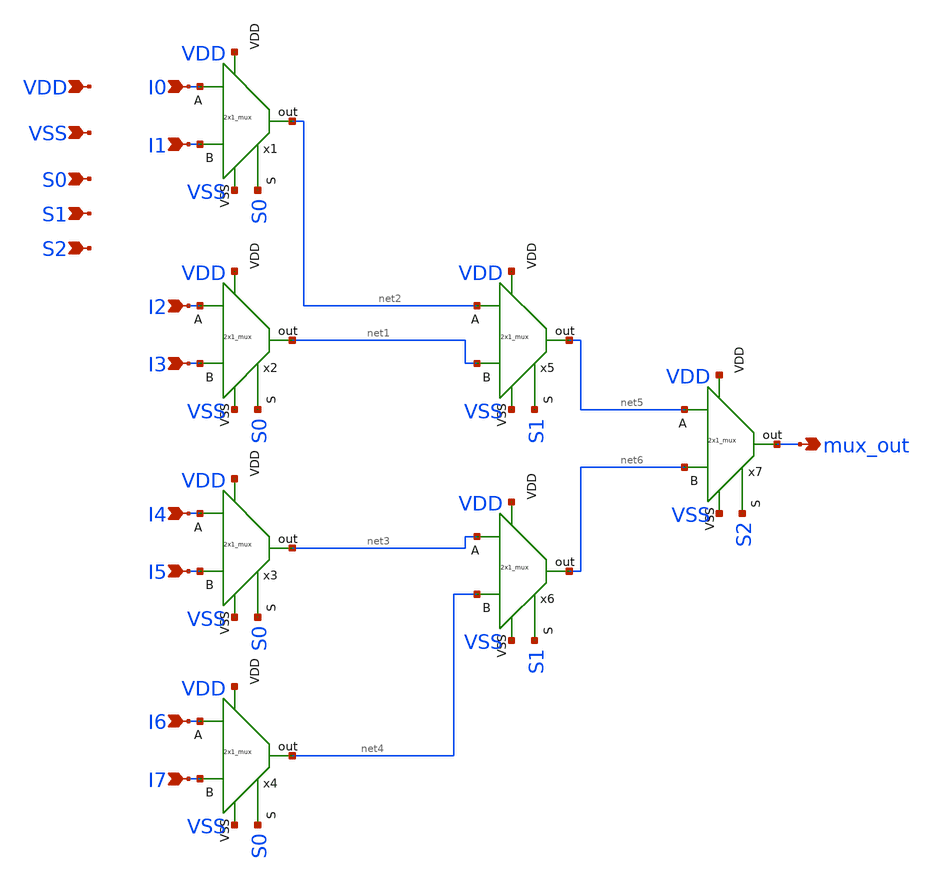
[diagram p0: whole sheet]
** sch_path: 8bit_mux.sch
**.subckt 8bit_mux I0 I1 I2 I3 I4 I5 I6 I7 VDD VSS S0 S1 S2 mux_out
*.ipin I0
*.ipin I1
*.ipin I2
*.ipin I3
*.ipin I4
*.ipin I5
*.ipin I6
*.ipin I7
*.ipin VDD
*.ipin VSS
*.ipin S0
*.ipin S1
*.ipin S2
*.opin mux_out
x1 I1 VDD I0 VSS S0 net2 2x1_mux
x2 I3 VDD I2 VSS S0 net1 2x1_mux
x3 I5 VDD I4 VSS S0 net3 2x1_mux
x4 I7 VDD I6 VSS S0 net4 2x1_mux
x5 net1 VDD net2 VSS S1 net5 2x1_mux
x6 net4 VDD net3 VSS S1 net6 2x1_mux
x7 net6 VDD net5 VSS S2 mux_out 2x1_mux
**.ends

* expanding   symbol:  2x1_mux/2x1_mux.sym # of pins=6
** sym_path: 2x1_mux/2x1_mux.sym
** sch_path: 2x1_mux/2x1_mux.sch
.subckt 2x1_mux B VDD A VSS S out
*.ipin VDD
*.ipin A
*.ipin B
*.opin out
*.ipin S
*.ipin VSS
XM1 net1 A net4 net4 sky130_fd_pr__nfet_01v8 L=0.15 W=1 nf=1 ad='int((nf+1)/2) * W/nf * 0.29' as='int((nf+2)/2) * W/nf * 0.29'
+ pd='2*int((nf+1)/2) * (W/nf + 0.29)' ps='2*int((nf+2)/2) * (W/nf + 0.29)' nrd='0.29 / W' nrs='0.29 / W'
+ sa=0 sb=0 sd=0 mult=1 m=1
XM2 net3 A VDD VDD sky130_fd_pr__pfet_01v8 L=0.15 W=1 nf=1 ad='int((nf+1)/2) * W/nf * 0.29' as='int((nf+2)/2) * W/nf * 0.29'
+ pd='2*int((nf+1)/2) * (W/nf + 0.29)' ps='2*int((nf+2)/2) * (W/nf + 0.29)' nrd='0.29 / W' nrs='0.29 / W'
+ sa=0 sb=0 sd=0 mult=1 m=1
XM3 net2 notS VDD VDD sky130_fd_pr__pfet_01v8 L=0.15 W=1 nf=1 ad='int((nf+1)/2) * W/nf * 0.29' as='int((nf+2)/2) * W/nf * 0.29'
+ pd='2*int((nf+1)/2) * (W/nf + 0.29)' ps='2*int((nf+2)/2) * (W/nf + 0.29)' nrd='0.29 / W' nrs='0.29 / W'
+ sa=0 sb=0 sd=0 mult=1 m=1
XM4 net1 B net3 net3 sky130_fd_pr__pfet_01v8 L=0.15 W=1 nf=1 ad='int((nf+1)/2) * W/nf * 0.29' as='int((nf+2)/2) * W/nf * 0.29'
+ pd='2*int((nf+1)/2) * (W/nf + 0.29)' ps='2*int((nf+2)/2) * (W/nf + 0.29)' nrd='0.29 / W' nrs='0.29 / W'
+ sa=0 sb=0 sd=0 mult=1 m=1
XM5 net1 S net2 net2 sky130_fd_pr__pfet_01v8 L=0.15 W=1 nf=1 ad='int((nf+1)/2) * W/nf * 0.29' as='int((nf+2)/2) * W/nf * 0.29'
+ pd='2*int((nf+1)/2) * (W/nf + 0.29)' ps='2*int((nf+2)/2) * (W/nf + 0.29)' nrd='0.29 / W' nrs='0.29 / W'
+ sa=0 sb=0 sd=0 mult=1 m=1
XM6 net1 B net5 net5 sky130_fd_pr__nfet_01v8 L=0.15 W=1 nf=1 ad='int((nf+1)/2) * W/nf * 0.29' as='int((nf+2)/2) * W/nf * 0.29'
+ pd='2*int((nf+1)/2) * (W/nf + 0.29)' ps='2*int((nf+2)/2) * (W/nf + 0.29)' nrd='0.29 / W' nrs='0.29 / W'
+ sa=0 sb=0 sd=0 mult=1 m=1
XM7 net4 notS VSS VSS sky130_fd_pr__nfet_01v8 L=0.15 W=1 nf=1 ad='int((nf+1)/2) * W/nf * 0.29' as='int((nf+2)/2) * W/nf * 0.29'
+ pd='2*int((nf+1)/2) * (W/nf + 0.29)' ps='2*int((nf+2)/2) * (W/nf + 0.29)' nrd='0.29 / W' nrs='0.29 / W'
+ sa=0 sb=0 sd=0 mult=1 m=1
XM8 net5 S VSS VSS sky130_fd_pr__nfet_01v8 L=0.15 W=1 nf=1 ad='int((nf+1)/2) * W/nf * 0.29' as='int((nf+2)/2) * W/nf * 0.29'
+ pd='2*int((nf+1)/2) * (W/nf + 0.29)' ps='2*int((nf+2)/2) * (W/nf + 0.29)' nrd='0.29 / W' nrs='0.29 / W'
+ sa=0 sb=0 sd=0 mult=1 m=1
XM9 notS S VSS VSS sky130_fd_pr__nfet_01v8 L=0.15 W=1 nf=1 ad='int((nf+1)/2) * W/nf * 0.29' as='int((nf+2)/2) * W/nf * 0.29'
+ pd='2*int((nf+1)/2) * (W/nf + 0.29)' ps='2*int((nf+2)/2) * (W/nf + 0.29)' nrd='0.29 / W' nrs='0.29 / W'
+ sa=0 sb=0 sd=0 mult=1 m=1
XM10 notS S VDD VDD sky130_fd_pr__pfet_01v8 L=0.15 W=1 nf=1 ad='int((nf+1)/2) * W/nf * 0.29' as='int((nf+2)/2) * W/nf * 0.29'
+ pd='2*int((nf+1)/2) * (W/nf + 0.29)' ps='2*int((nf+2)/2) * (W/nf + 0.29)' nrd='0.29 / W' nrs='0.29 / W'
+ sa=0 sb=0 sd=0 mult=1 m=1
XM11 out net1 VSS VSS sky130_fd_pr__nfet_01v8 L=0.15 W=1 nf=1 ad='int((nf+1)/2) * W/nf * 0.29' as='int((nf+2)/2) * W/nf * 0.29'
+ pd='2*int((nf+1)/2) * (W/nf + 0.29)' ps='2*int((nf+2)/2) * (W/nf + 0.29)' nrd='0.29 / W' nrs='0.29 / W'
+ sa=0 sb=0 sd=0 mult=1 m=1
XM12 out net1 VDD VDD sky130_fd_pr__pfet_01v8 L=0.15 W=1 nf=1 ad='int((nf+1)/2) * W/nf * 0.29' as='int((nf+2)/2) * W/nf * 0.29'
+ pd='2*int((nf+1)/2) * (W/nf + 0.29)' ps='2*int((nf+2)/2) * (W/nf + 0.29)' nrd='0.29 / W' nrs='0.29 / W'
+ sa=0 sb=0 sd=0 mult=1 m=1
.ends

.end
